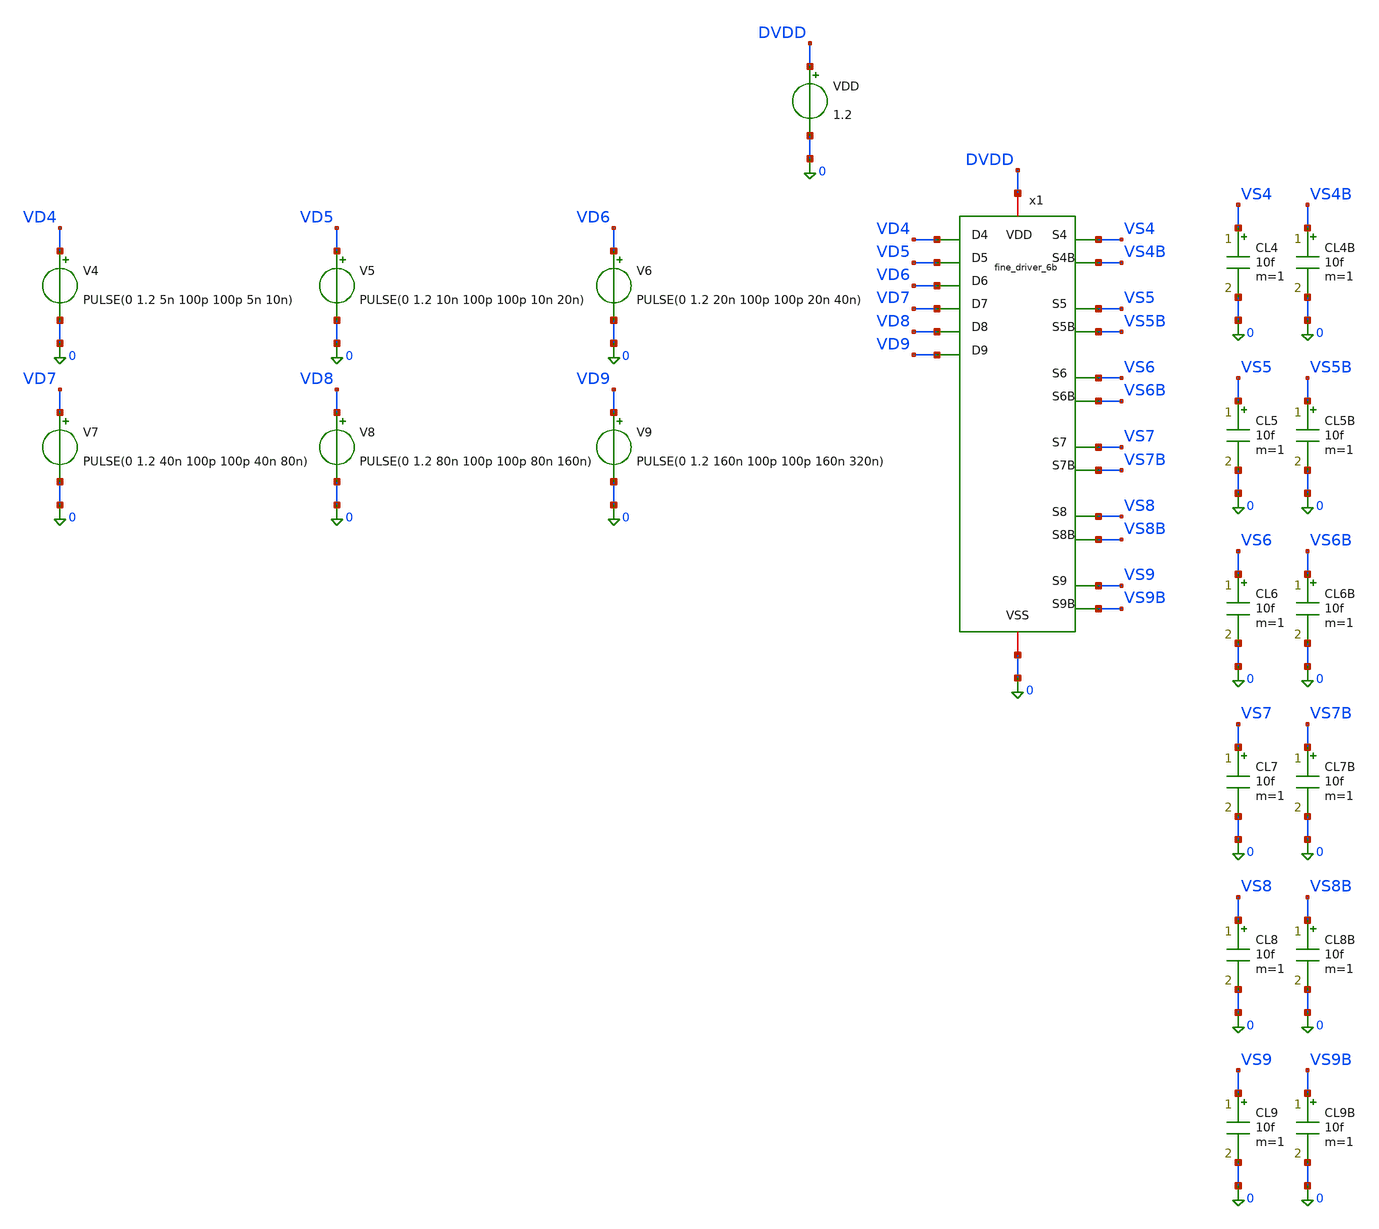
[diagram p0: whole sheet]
** sch_path: designs/archives/fine_driver_6b/tb_fine_driver_6b.sch
**.subckt tb_fine_driver_6b
x1 VD4 VD7 VS4 VS4B DVDD 0 VD5 VD6 VD8 VD9 VS5 VS5B VS6 VS6B VS7 VS7B VS8 VS8B VS9 VS9B
+ fine_driver_6b
VDD DVDD 0 1.2
V6 VD6 0 PULSE(0 1.2 20n 100p 100p 20n 40n)
V5 VD5 0 PULSE(0 1.2 10n 100p 100p 10n 20n)
V4 VD4 0 PULSE(0 1.2 5n 100p 100p 5n 10n)
V7 VD7 0 PULSE(0 1.2 40n 100p 100p 40n 80n)
V8 VD8 0 PULSE(0 1.2 80n 100p 100p 80n 160n)
V9 VD9 0 PULSE(0 1.2 160n 100p 100p 160n 320n)
CL4 VS4 0 10f m=1
CL4B VS4B 0 10f m=1
CL5 VS5 0 10f m=1
CL5B VS5B 0 10f m=1
CL6 VS6 0 10f m=1
CL6B VS6B 0 10f m=1
CL7 VS7 0 10f m=1
CL7B VS7B 0 10f m=1
CL8 VS8 0 10f m=1
CL8B VS8B 0 10f m=1
CL9 VS9 0 10f m=1
CL9B VS9B 0 10f m=1
**** begin user architecture code

.lib cornerMOSlv.lib mos_tt
.include /foss/pdks/ihp-sg13cmos5l/libs.ref/sg13cmos5l_stdcell/spice/sg13cmos5l_stdcell.spice


.control
  tran 100p 320n
  write tb_fine_driver_6b.raw

  * Multi-trace offset plots for Lower 3 bits (D4, D5, D6)
  plot v(VD4) v(VS4)+1.5 v(VS4B)+3.0 title 'Bit 4: Input (VD4), True (VS4), Complement (VS4B)' xlabel
+ 'Time (s)' ylabel 'Voltage (V)'
  plot v(VD5) v(VS5)+1.5 v(VS5B)+3.0 title 'Bit 5: Input (VD5), True (VS5), Complement (VS5B)' xlabel
+ 'Time (s)' ylabel 'Voltage (V)'
  plot v(VD6) v(VS6)+1.5 v(VS6B)+3.0 title 'Bit 6: Input (VD6), True (VS6), Complement (VS6B)' xlabel
+ 'Time (s)' ylabel 'Voltage (V)'

  * Multi-trace offset plots for Upper 3 bits (D7, D8, D9)
  plot v(VD7) v(VS7)+1.5 v(VS7B)+3.0 title 'Bit 7: Input (VD7), True (VS7), Complement (VS7B)' xlabel
+ 'Time (s)' ylabel 'Voltage (V)'
  plot v(VD8) v(VS8)+1.5 v(VS8B)+3.0 title 'Bit 8: Input (VD8), True (VS8), Complement (VS8B)' xlabel
+ 'Time (s)' ylabel 'Voltage (V)'
  plot v(VD9) v(VS9)+1.5 v(VS9B)+3.0 title 'Bit 9: Input (VD9), True (VS9), Complement (VS9B)' xlabel
+ 'Time (s)' ylabel 'Voltage (V)'
.endc


**** end user architecture code
**.ends
.end
